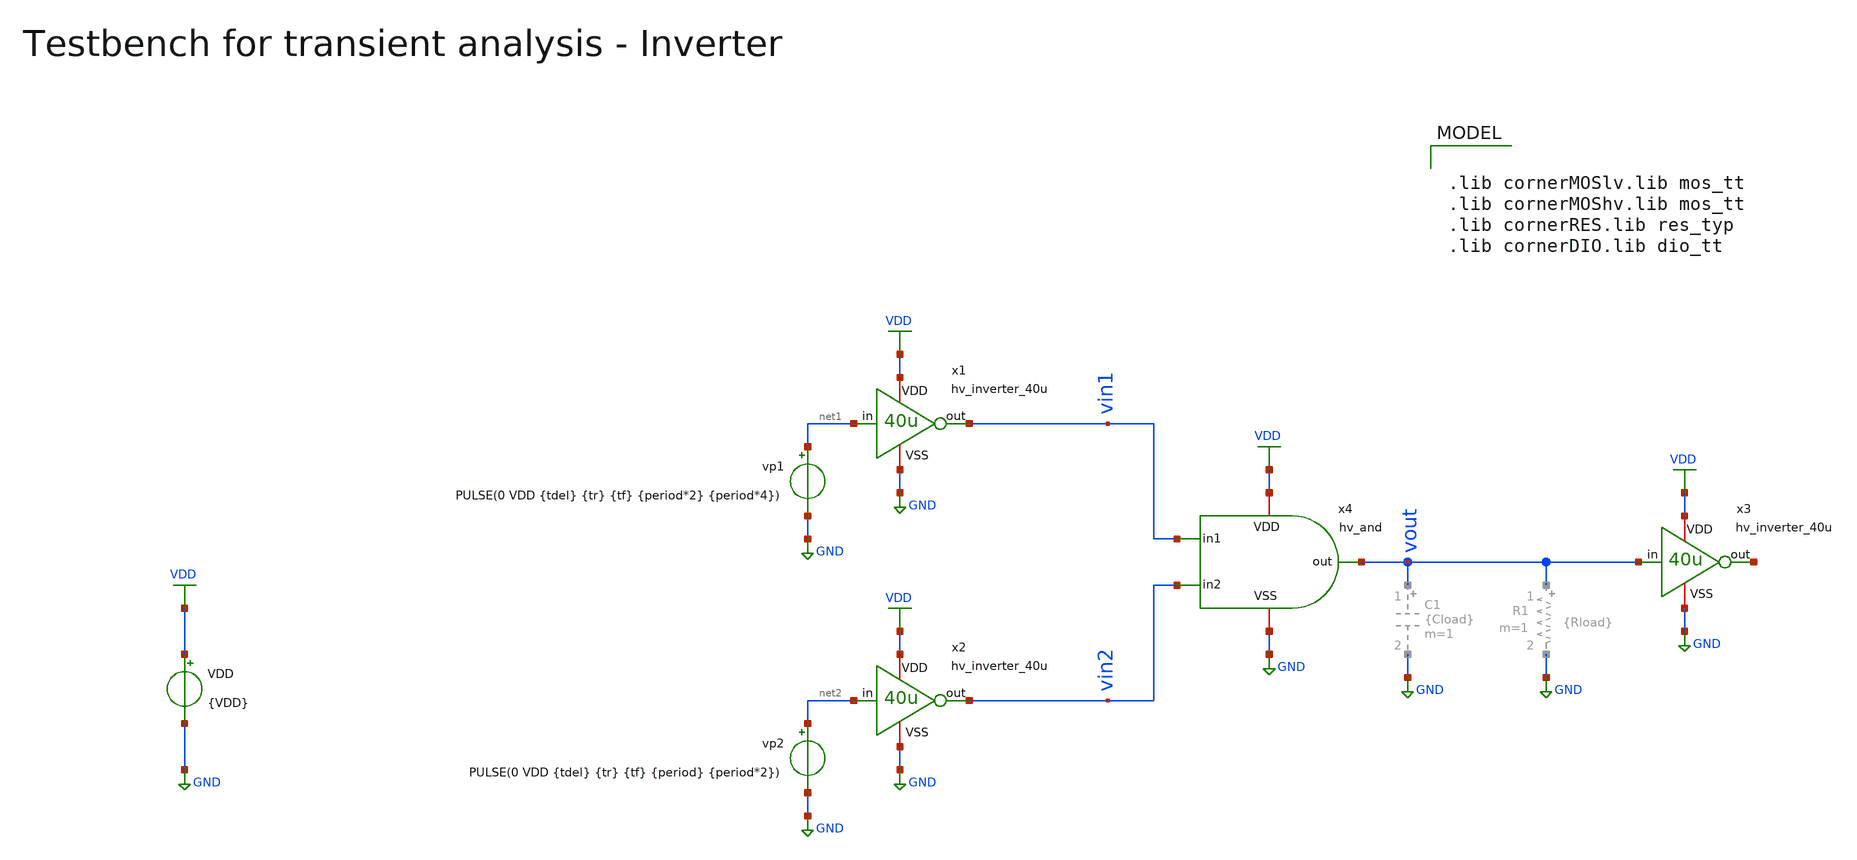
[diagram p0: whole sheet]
** sch_path: macros/heichips26_vcr/macros/switched_capacitor/testbenches/xschem/tb_hv_and_tran.sch
**.subckt tb_hv_and_tran
VDD VDD GND {VDD}
vp2 net2 GND PULSE(0 VDD {tdel} {tr} {tf} {period} {period*2})
vp1 net1 GND PULSE(0 VDD {tdel} {tr} {tf} {period*2} {period*4})
x1 VDD net1 vin1 GND hv_inverter_40u
x2 VDD net2 vin2 GND hv_inverter_40u
x3 VDD vout net3 GND hv_inverter_40u
x4 VDD vin1 vout vin2 GND hv_and
**** begin user architecture code


.param VDD=3.3
.csparam VDD=VDD
.param Vcm=VDD/2
.param temp=27
.param Cload=10p
.param Rload=1k

.param period = 1n
.param tdel   = {period/2}
.param ton    = {period*2}
.csparam tstop  = {5*period}
.csparam tstep  = {period/100}
.param tr     = {period/100}
.param tf     = {period/100}

.options savecurrents klu method=gear reltol=1e-4 abstol=1e-15 gmin=1e-15
.control

save all

* Operating Point Analysis
op
remzerovec
write @schname\.raw
set appendwrite

* Transient Analysis
tran {$&tstep} {$&tstop}
write @schname\.raw

* Plotting
plot vin1+8 vin2+4 vout

* Write Data
unset appendwrite
set wr_vecnames
set wr_singlescale
wrdata ../plot_simulations/data/@schname\.txt v(vin1) v(vin2) v(vout)

*quit
.endc



.lib cornerMOSlv.lib mos_tt
.lib cornerMOShv.lib mos_tt
.lib cornerRES.lib res_typ
.lib cornerDIO.lib dio_tt

**** end user architecture code
**.ends

* expanding   symbol:  hv_inverter_40u.sym # of pins=4
** sym_path: macros/heichips26_vcr/macros/switched_capacitor/schematic/xschem/hv_inverter_40u.sym
** sch_path: macros/heichips26_vcr/macros/switched_capacitor/schematic/xschem/hv_inverter_40u.sch
.subckt hv_inverter_40u VDD in out VSS
*.ipin in
*.iopin VDD
*.iopin VSS
*.opin out
XM2 out in VSS VSS sg13_hv_nmos w={n_w} l={n_l} ng={ng} m=1 mm_ok=1
XM3 out in VDD VDD sg13_hv_pmos w={p_w} l={p_l} ng={ng} m=1 mm_ok=1
**** begin user architecture code


.param w   = 10u
.param ng  = 4
.param n_ng = ng
.param n_w = {3u*n_ng}
.param n_l = 0.45u
.param p_ng = ng
.param p_w = {10u*p_ng}
.param p_l = 0.4u


**** end user architecture code
.ends


* expanding   symbol:  hv_and.sym # of pins=5
** sym_path: macros/heichips26_vcr/macros/switched_capacitor/schematic/xschem/hv_and.sym
** sch_path: macros/heichips26_vcr/macros/switched_capacitor/schematic/xschem/hv_and.sch
.subckt hv_and VDD in1 out in2 VSS
*.ipin in1
*.iopin VDD
*.iopin VSS
*.opin out
*.ipin in2
**** begin user architecture code


.param w   = 10u
.param ng  = 4
.param n_ng = ng
.param n_w = {3u*n_ng}
.param n_l = 0.45u
.param p_ng = ng
.param p_w = {10u*p_ng}
.param p_l = 0.4u


**** end user architecture code
x4 VDD in1 net1 in2 VSS hv_nand
x1 VDD net1 out VSS hv_inverter_40u
.ends


* expanding   symbol:  hv_nand.sym # of pins=5
** sym_path: macros/heichips26_vcr/macros/switched_capacitor/schematic/xschem/hv_nand.sym
** sch_path: macros/heichips26_vcr/macros/switched_capacitor/schematic/xschem/hv_nand.sch
.subckt hv_nand VDD in1 out in2 VSS
*.ipin in1
*.iopin VDD
*.iopin VSS
*.opin out
*.ipin in2
**** begin user architecture code


.param w   = 10u
.param ng  = 4
.param n_ng = ng
.param n_w = {3u*n_ng}
.param n_l = 0.45u
.param p_ng = ng
.param p_w = {10u*p_ng}
.param p_l = 0.4u


**** end user architecture code
XM2 out in1 net1 VSS sg13_hv_nmos w={n_w} l={n_l} ng={ng} m=1 mm_ok=1
XM3 out in2 VDD VDD sg13_hv_pmos w={p_w} l={p_l} ng={ng} m=1 mm_ok=1
XM1 net1 in2 VSS VSS sg13_hv_nmos w={n_w} l={n_l} ng={ng} m=1 mm_ok=1
XM4 out in1 VDD VDD sg13_hv_pmos w={p_w} l={p_l} ng={ng} m=1 mm_ok=1
.ends

.GLOBAL GND
.GLOBAL VDD
.end
